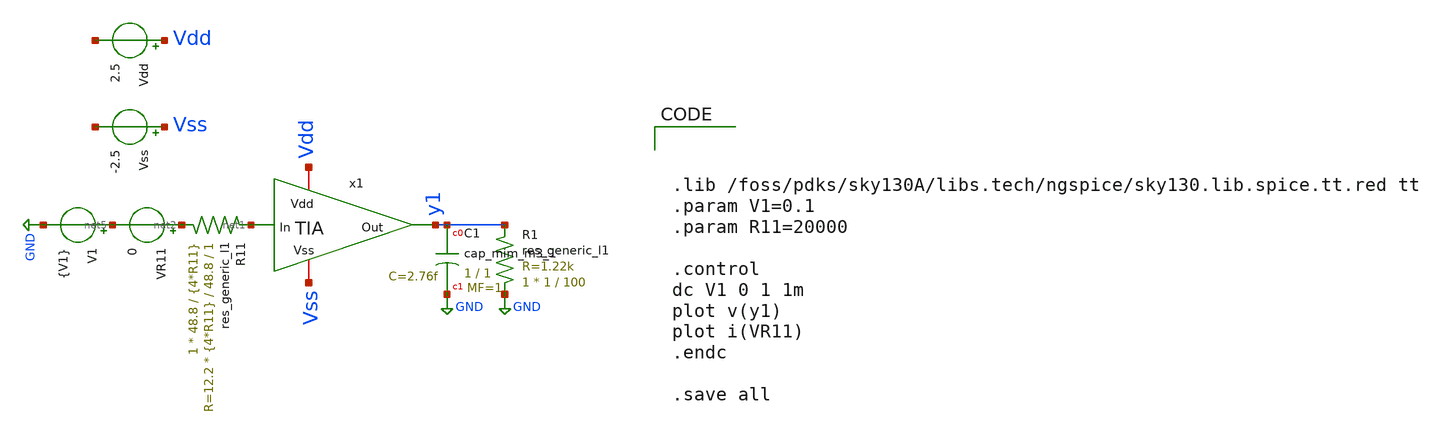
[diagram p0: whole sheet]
** sch_path: Vector-Matrix-Multiplicaction/xschem/VMM_Experiment.sch
**.subckt VMM_Experiment
x1 Vdd net1 y1 Vss TIA
R11 net2 net1 sky130_fd_pr__res_generic_l1 W=48.8 L={4*R11} m=1
Vdd Vdd net3 2.5
Vss Vss net4 -2.5
V1 net5 GND {V1}
VR11 net2 net5 0
R1 GND y1 sky130_fd_pr__res_generic_l1 W=1 L=100 m=1
XC1 y1 GND sky130_fd_pr__cap_mim_m3_1 W=1 L=1 MF=1 m=1
**** begin user architecture code



.lib /foss/pdks/sky130A/libs.tech/ngspice/sky130.lib.spice.tt.red tt
.param V1=0.1
.param R11=20000

.control
dc V1 0 1 1m
plot v(y1)
plot i(VR11)
.endc

.save all



**** end user architecture code
**.ends

* expanding   symbol:  /foss/designs/ProyectoChipUSM/TIA.sym # of pins=4
** sym_path: Vector-Matrix-Multiplicaction/xschem/TIA.sym
** sch_path: Vector-Matrix-Multiplicaction/xschem/TIA.sch
.subckt TIA Vdd In Out Vss
*.ipin In
*.opin Out
*.iopin Vdd
*.iopin Vss
Rf1 In Out sky130_fd_pr__res_generic_l1 W=48.8 L=20000 m=1
XMp Out In Vdd Vdd sky130_fd_pr__pfet_g5v0d10v5 L=1 W=15 nf=1 ad='int((nf+1)/2) * W/nf * 0.29' as='int((nf+2)/2) * W/nf * 0.29'
+ pd='2*int((nf+1)/2) * (W/nf + 0.29)' ps='2*int((nf+2)/2) * (W/nf + 0.29)' nrd='0.29 / W' nrs='0.29 / W'
+ sa=0 sb=0 sd=0 mult=1 m=1
XMn Out In Vss Vss sky130_fd_pr__nfet_g5v0d10v5 L=1 W=5 nf=1 ad='int((nf+1)/2) * W/nf * 0.29' as='int((nf+2)/2) * W/nf * 0.29'
+ pd='2*int((nf+1)/2) * (W/nf + 0.29)' ps='2*int((nf+2)/2) * (W/nf + 0.29)' nrd='0.29 / W' nrs='0.29 / W'
+ sa=0 sb=0 sd=0 mult=1 m=1
.ends

.GLOBAL GND
.end
